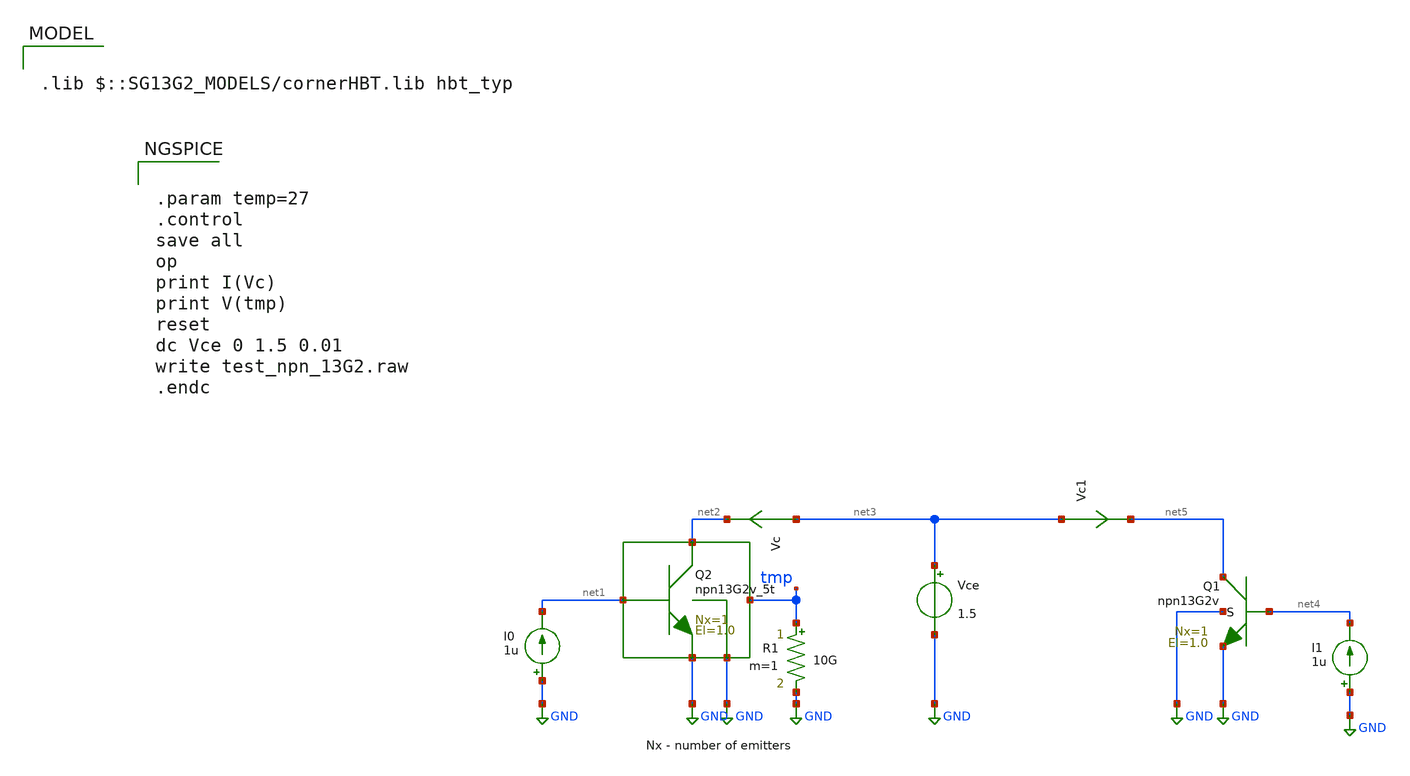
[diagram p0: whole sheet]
** sch_path: ihp-sg13g2/libs.tech/xschem/sg13g2_tests/dc_hbt_13g2v_5t.sch
* Copyright 2023 IHP PDK Authors
**.subckt dc_hbt_13g2v_5t
Vce net3 GND 1.5
I0 GND net1 1u
Vc net3 net2 0
.save i(vc)
R1 tmp GND 10G m=1
I1 GND net4 1u
Vc1 net3 net5 0
.save i(vc1)
XQ1 net5 net4 GND GND npn13G2v Nx=1 El=1.0 mm_ok=1
XQ2 net2 net1 GND GND tmp npn13G2v_5t Nx=1 El=1.0 mm_ok=1
**** begin user architecture code

.lib $::SG13G2_MODELS/cornerHBT.lib hbt_typ



.param temp=27
.control
save all
op
print I(Vc)
print V(tmp)
reset
dc Vce 0 1.5 0.01
write test_npn_13G2.raw
.endc


**** end user architecture code
**.ends
.GLOBAL GND
.end
